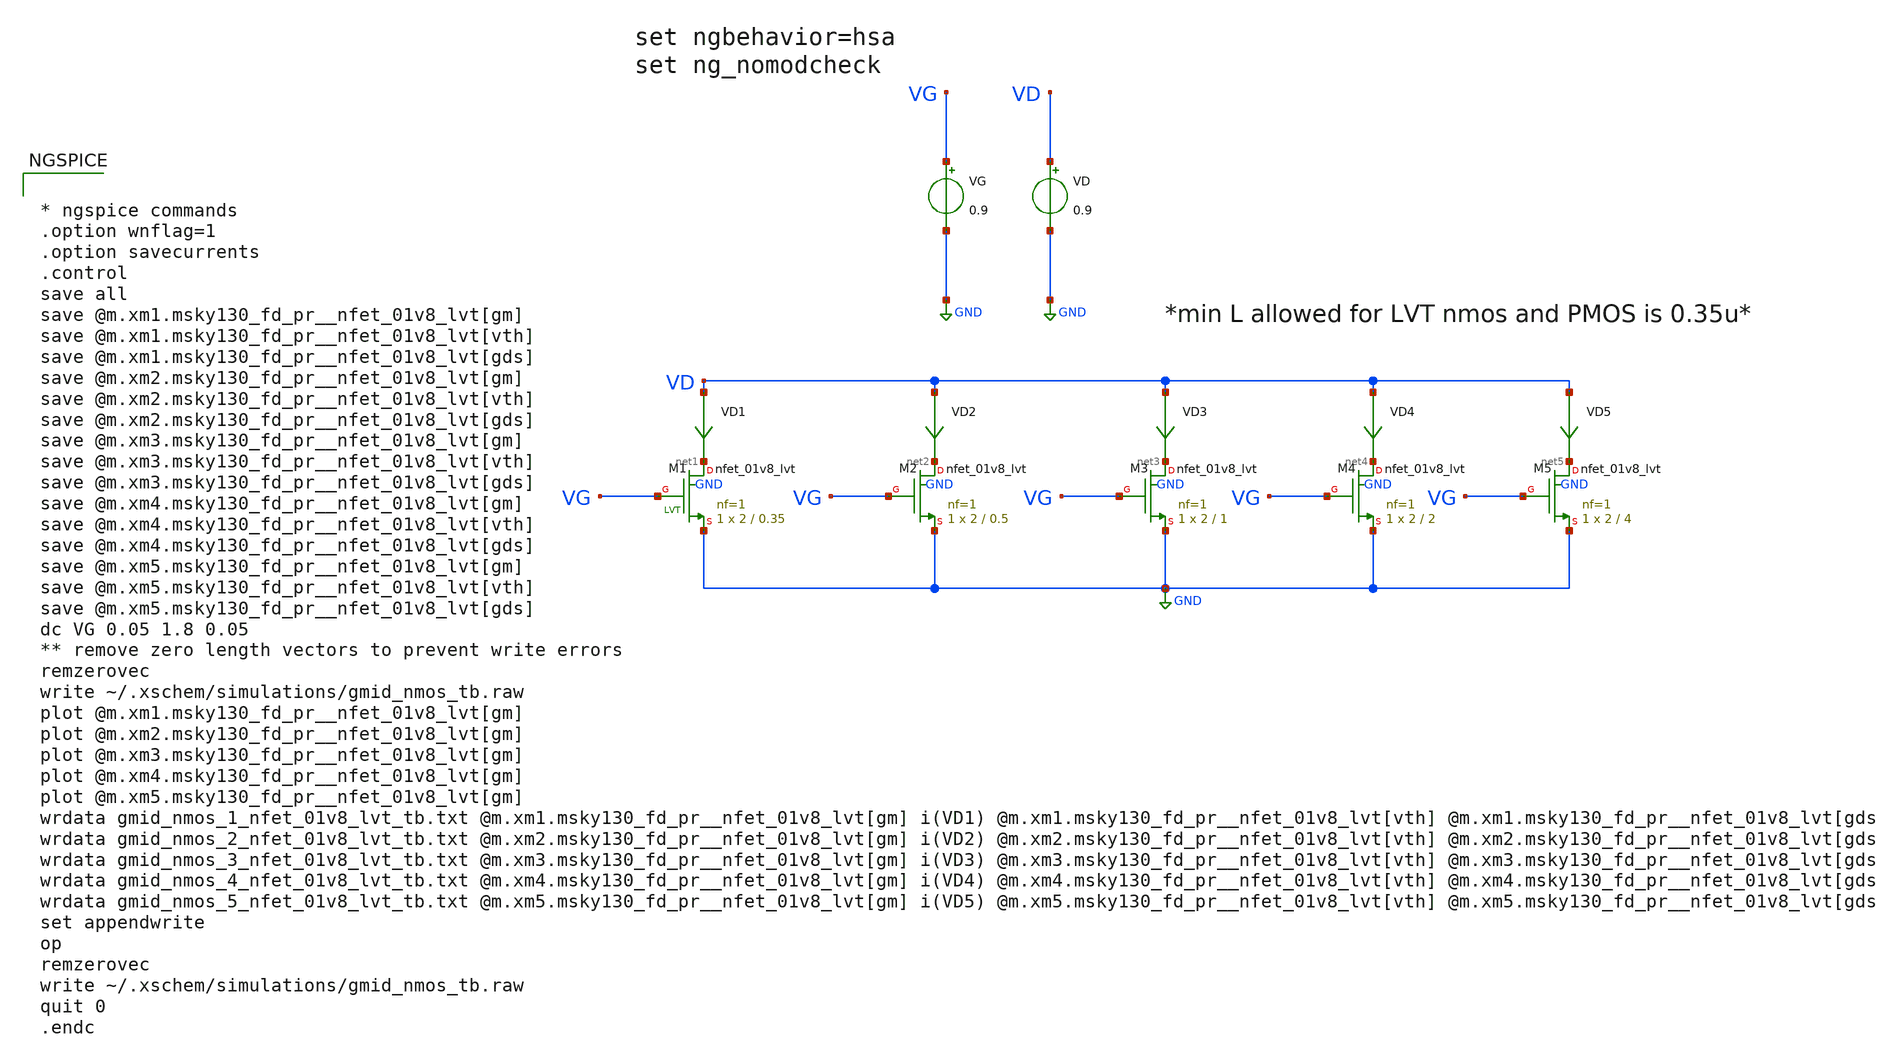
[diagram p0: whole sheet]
** sch_path: designs/gmid_nmos_1v8_lvt_tb.sch
**.subckt gmid_nmos_1v8_lvt_tb
VG VG GND 0.9
VD VD GND 0.9
XM1 net1 VG GND GND sky130_fd_pr__nfet_01v8_lvt L=0.35 W=2 nf=1 ad='int((nf+1)/2) * W/nf * 0.29' as='int((nf+2)/2) * W/nf * 0.29'
+ pd='2*int((nf+1)/2) * (W/nf + 0.29)' ps='2*int((nf+2)/2) * (W/nf + 0.29)' nrd='0.29 / W' nrs='0.29 / W'
+ sa=0 sb=0 sd=0 mult=1 m=1
XM2 net2 VG GND GND sky130_fd_pr__nfet_01v8_lvt L=0.5 W=2 nf=1 ad='int((nf+1)/2) * W/nf * 0.29' as='int((nf+2)/2) * W/nf * 0.29'
+ pd='2*int((nf+1)/2) * (W/nf + 0.29)' ps='2*int((nf+2)/2) * (W/nf + 0.29)' nrd='0.29 / W' nrs='0.29 / W'
+ sa=0 sb=0 sd=0 mult=1 m=1
XM3 net3 VG GND GND sky130_fd_pr__nfet_01v8_lvt L=1 W=2 nf=1 ad='int((nf+1)/2) * W/nf * 0.29' as='int((nf+2)/2) * W/nf * 0.29'
+ pd='2*int((nf+1)/2) * (W/nf + 0.29)' ps='2*int((nf+2)/2) * (W/nf + 0.29)' nrd='0.29 / W' nrs='0.29 / W'
+ sa=0 sb=0 sd=0 mult=1 m=1
XM4 net4 VG GND GND sky130_fd_pr__nfet_01v8_lvt L=2 W=2 nf=1 ad='int((nf+1)/2) * W/nf * 0.29' as='int((nf+2)/2) * W/nf * 0.29'
+ pd='2*int((nf+1)/2) * (W/nf + 0.29)' ps='2*int((nf+2)/2) * (W/nf + 0.29)' nrd='0.29 / W' nrs='0.29 / W'
+ sa=0 sb=0 sd=0 mult=1 m=1
XM5 net5 VG GND GND sky130_fd_pr__nfet_01v8_lvt L=4 W=2 nf=1 ad='int((nf+1)/2) * W/nf * 0.29' as='int((nf+2)/2) * W/nf * 0.29'
+ pd='2*int((nf+1)/2) * (W/nf + 0.29)' ps='2*int((nf+2)/2) * (W/nf + 0.29)' nrd='0.29 / W' nrs='0.29 / W'
+ sa=0 sb=0 sd=0 mult=1 m=1
VD1 VD net1 0
.save i(vd1)
VD2 VD net2 0
.save i(vd2)
VD3 VD net3 0
.save i(vd3)
VD4 VD net4 0
.save i(vd4)
VD5 VD net5 0
.save i(vd5)
**** begin user architecture code

** opencircuitdesign pdks install
.lib $::SKYWATER_MODELS/sky130.lib.spice ff




* ngspice commands
.option wnflag=1
.option savecurrents
.control
save all
save @m.xm1.msky130_fd_pr__nfet_01v8_lvt[gm]
save @m.xm1.msky130_fd_pr__nfet_01v8_lvt[vth]
save @m.xm1.msky130_fd_pr__nfet_01v8_lvt[gds]
save @m.xm2.msky130_fd_pr__nfet_01v8_lvt[gm]
save @m.xm2.msky130_fd_pr__nfet_01v8_lvt[vth]
save @m.xm2.msky130_fd_pr__nfet_01v8_lvt[gds]
save @m.xm3.msky130_fd_pr__nfet_01v8_lvt[gm]
save @m.xm3.msky130_fd_pr__nfet_01v8_lvt[vth]
save @m.xm3.msky130_fd_pr__nfet_01v8_lvt[gds]
save @m.xm4.msky130_fd_pr__nfet_01v8_lvt[gm]
save @m.xm4.msky130_fd_pr__nfet_01v8_lvt[vth]
save @m.xm4.msky130_fd_pr__nfet_01v8_lvt[gds]
save @m.xm5.msky130_fd_pr__nfet_01v8_lvt[gm]
save @m.xm5.msky130_fd_pr__nfet_01v8_lvt[vth]
save @m.xm5.msky130_fd_pr__nfet_01v8_lvt[gds]
dc VG 0.05 1.8 0.05
** remove zero length vectors to prevent write errors
remzerovec
write ~/.xschem/simulations/gmid_nmos_tb.raw
plot @m.xm1.msky130_fd_pr__nfet_01v8_lvt[gm]
plot @m.xm2.msky130_fd_pr__nfet_01v8_lvt[gm]
plot @m.xm3.msky130_fd_pr__nfet_01v8_lvt[gm]
plot @m.xm4.msky130_fd_pr__nfet_01v8_lvt[gm]
plot @m.xm5.msky130_fd_pr__nfet_01v8_lvt[gm]
wrdata gmid_nmos_1_nfet_01v8_lvt_tb.txt @m.xm1.msky130_fd_pr__nfet_01v8_lvt[gm] i(VD1)
+ @m.xm1.msky130_fd_pr__nfet_01v8_lvt[vth] @m.xm1.msky130_fd_pr__nfet_01v8_lvt[gds]
wrdata gmid_nmos_2_nfet_01v8_lvt_tb.txt @m.xm2.msky130_fd_pr__nfet_01v8_lvt[gm] i(VD2)
+ @m.xm2.msky130_fd_pr__nfet_01v8_lvt[vth] @m.xm2.msky130_fd_pr__nfet_01v8_lvt[gds]
wrdata gmid_nmos_3_nfet_01v8_lvt_tb.txt @m.xm3.msky130_fd_pr__nfet_01v8_lvt[gm] i(VD3)
+ @m.xm3.msky130_fd_pr__nfet_01v8_lvt[vth] @m.xm3.msky130_fd_pr__nfet_01v8_lvt[gds]
wrdata gmid_nmos_4_nfet_01v8_lvt_tb.txt @m.xm4.msky130_fd_pr__nfet_01v8_lvt[gm] i(VD4)
+ @m.xm4.msky130_fd_pr__nfet_01v8_lvt[vth] @m.xm4.msky130_fd_pr__nfet_01v8_lvt[gds]
wrdata gmid_nmos_5_nfet_01v8_lvt_tb.txt @m.xm5.msky130_fd_pr__nfet_01v8_lvt[gm] i(VD5)
+ @m.xm5.msky130_fd_pr__nfet_01v8_lvt[vth] @m.xm5.msky130_fd_pr__nfet_01v8_lvt[gds]
set appendwrite
op
remzerovec
write ~/.xschem/simulations/gmid_nmos_tb.raw
quit 0
.endc


**** end user architecture code
**.ends
.GLOBAL GND
.end
